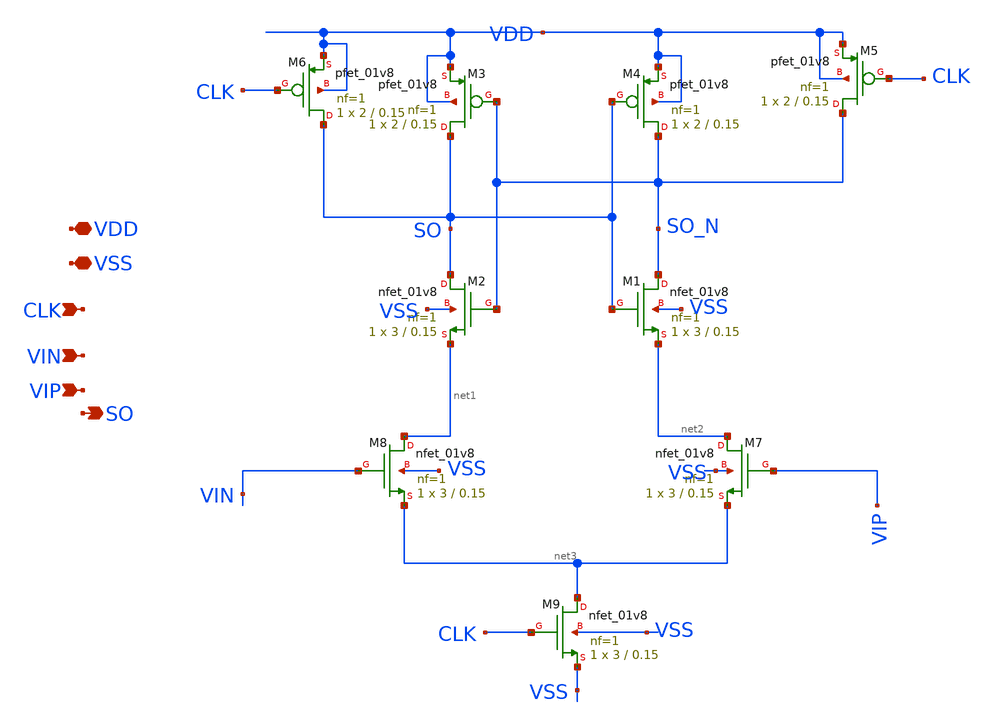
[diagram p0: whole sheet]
** sch_path: xschem/Integrated_bitcell/Sense_Amplifier.sch
**.subckt Sense_Amplifier VDD VSS CLK VIN VIP SO
*.iopin VDD
*.iopin VSS
*.ipin CLK
*.ipin VIN
*.ipin VIP
*.opin SO
XM1 SO_N SO net2 VSS sky130_fd_pr__nfet_01v8 L=0.15 W=3 nf=1 ad='int((nf+1)/2) * W/nf * 0.29' as='int((nf+2)/2) * W/nf * 0.29'
+ pd='2*int((nf+1)/2) * (W/nf + 0.29)' ps='2*int((nf+2)/2) * (W/nf + 0.29)' nrd='0.29 / W' nrs='0.29 / W'
+ sa=0 sb=0 sd=0 mult=1 m=1
XM2 SO SO_N net1 VSS sky130_fd_pr__nfet_01v8 L=0.15 W=3 nf=1 ad='int((nf+1)/2) * W/nf * 0.29' as='int((nf+2)/2) * W/nf * 0.29'
+ pd='2*int((nf+1)/2) * (W/nf + 0.29)' ps='2*int((nf+2)/2) * (W/nf + 0.29)' nrd='0.29 / W' nrs='0.29 / W'
+ sa=0 sb=0 sd=0 mult=1 m=1
XM3 SO SO_N VDD VDD sky130_fd_pr__pfet_01v8 L=0.15 W=2 nf=1 ad='int((nf+1)/2) * W/nf * 0.29' as='int((nf+2)/2) * W/nf * 0.29'
+ pd='2*int((nf+1)/2) * (W/nf + 0.29)' ps='2*int((nf+2)/2) * (W/nf + 0.29)' nrd='0.29 / W' nrs='0.29 / W'
+ sa=0 sb=0 sd=0 mult=1 m=1
XM4 SO_N SO VDD VDD sky130_fd_pr__pfet_01v8 L=0.15 W=2 nf=1 ad='int((nf+1)/2) * W/nf * 0.29' as='int((nf+2)/2) * W/nf * 0.29'
+ pd='2*int((nf+1)/2) * (W/nf + 0.29)' ps='2*int((nf+2)/2) * (W/nf + 0.29)' nrd='0.29 / W' nrs='0.29 / W'
+ sa=0 sb=0 sd=0 mult=1 m=1
XM5 SO_N CLK VDD VDD sky130_fd_pr__pfet_01v8 L=0.15 W=2 nf=1 ad='int((nf+1)/2) * W/nf * 0.29' as='int((nf+2)/2) * W/nf * 0.29'
+ pd='2*int((nf+1)/2) * (W/nf + 0.29)' ps='2*int((nf+2)/2) * (W/nf + 0.29)' nrd='0.29 / W' nrs='0.29 / W'
+ sa=0 sb=0 sd=0 mult=1 m=1
XM6 SO CLK VDD VDD sky130_fd_pr__pfet_01v8 L=0.15 W=2 nf=1 ad='int((nf+1)/2) * W/nf * 0.29' as='int((nf+2)/2) * W/nf * 0.29'
+ pd='2*int((nf+1)/2) * (W/nf + 0.29)' ps='2*int((nf+2)/2) * (W/nf + 0.29)' nrd='0.29 / W' nrs='0.29 / W'
+ sa=0 sb=0 sd=0 mult=1 m=1
XM7 net2 VIP net3 VSS sky130_fd_pr__nfet_01v8 L=0.15 W=3 nf=1 ad='int((nf+1)/2) * W/nf * 0.29' as='int((nf+2)/2) * W/nf * 0.29'
+ pd='2*int((nf+1)/2) * (W/nf + 0.29)' ps='2*int((nf+2)/2) * (W/nf + 0.29)' nrd='0.29 / W' nrs='0.29 / W'
+ sa=0 sb=0 sd=0 mult=1 m=1
XM8 net1 VIN net3 VSS sky130_fd_pr__nfet_01v8 L=0.15 W=3 nf=1 ad='int((nf+1)/2) * W/nf * 0.29' as='int((nf+2)/2) * W/nf * 0.29'
+ pd='2*int((nf+1)/2) * (W/nf + 0.29)' ps='2*int((nf+2)/2) * (W/nf + 0.29)' nrd='0.29 / W' nrs='0.29 / W'
+ sa=0 sb=0 sd=0 mult=1 m=1
XM9 net3 CLK VSS VSS sky130_fd_pr__nfet_01v8 L=0.15 W=3 nf=1 ad='int((nf+1)/2) * W/nf * 0.29' as='int((nf+2)/2) * W/nf * 0.29'
+ pd='2*int((nf+1)/2) * (W/nf + 0.29)' ps='2*int((nf+2)/2) * (W/nf + 0.29)' nrd='0.29 / W' nrs='0.29 / W'
+ sa=0 sb=0 sd=0 mult=1 m=1
**.ends
.end
